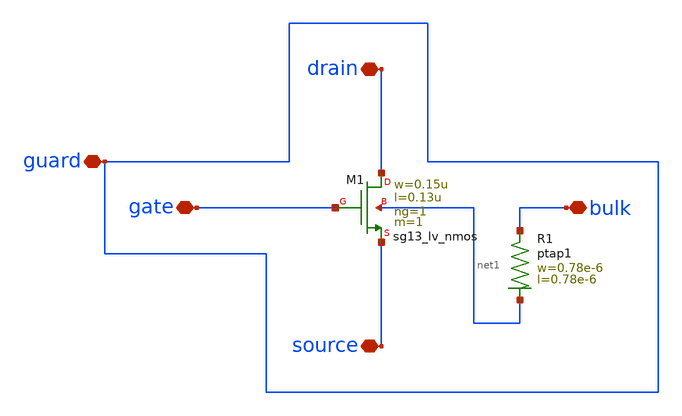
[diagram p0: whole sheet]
** sch_path: trident_test_structures/design_data/xschem/transistor_characterization/lv_nmos_w0u15_l0u13_guarded/lv_nmos_w0u15_l0u13_guarded.sch
**.subckt lv_nmos_w0u15_l0u13_guarded gate drain source bulk guard
*.iopin gate
*.iopin drain
*.iopin source
*.iopin bulk
*.iopin guard
XM1 drain gate source net1 sg13_lv_nmos w=0.15u l=0.13u ng=1 m=1 mm_ok=1
XR1 bulk net1 ptap1 R=262.8 w=0.78e-6 l=0.78e-6
**.ends
.end
